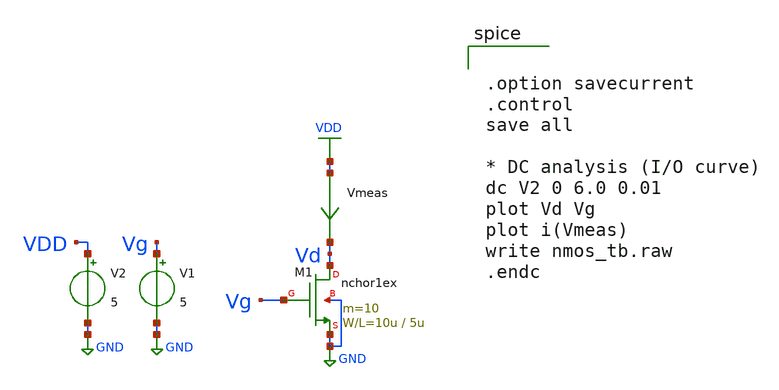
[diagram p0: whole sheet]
** sch_path: design/xschem/nmos.sch
**.subckt nmos
M1 Vd Vg GND GND nchor1ex L=5u W=10u m=10
Vmeas VDD Vd 0
.save i(vmeas)
V1 Vg GND 5
V2 VDD GND 5
**** begin user architecture code
 .include $::LIB/mos.lib
.include $::LIB/passive.lib
.include $::LIB/diode.lib


.option savecurrent
.control
save all

* DC analysis (I/O curve)
dc V2 0 6.0 0.01
plot Vd Vg
plot i(Vmeas)
write nmos_tb.raw
.endc

**** end user architecture code
**.ends
.GLOBAL GND
.GLOBAL VDD
.end
